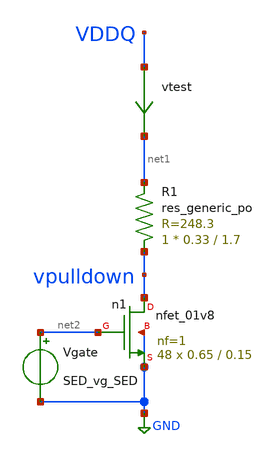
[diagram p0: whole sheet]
** sch_path: schem/test_pd_res.sch
* Copyright 2021 Stefan Frederik Schippers
* Licensed under the Apache License, Version 2.0 (the "License");
* you may not use this file except in compliance with the License.
* You may obtain a copy of the License at
* https://www.apache.org/licenses/LICENSE-2.0
* Unless required by applicable law or agreed to in writing, software
* distributed under the License is distributed on an "AS IS" BASIS,
* WITHOUT WARRANTIES OR CONDITIONS OF ANY KIND, either express or implied.
* See the License for the specific language governing permissions and
* limitations under the License.
**.subckt test_pd_res
XR1 vpulldown net1 sky130_fd_pr__res_generic_po W=0.33 L=1.7 m=1
vtest VDDQ net1 0
.save i(vtest)
Xn1 vpulldown net2 GND GND sky130_fd_pr__nfet_01v8 L=0.15 W=0.65 nf=1 ad='int((nf+1)/2) * W/nf * 0.29'
+ as='int((nf+2)/2) * W/nf * 0.29' pd='2*int((nf+1)/2) * (W/nf + 0.29)' ps='2*int((nf+2)/2) * (W/nf + 0.29)'
+ nrd='0.29 / W' nrs='0.29 / W' sa=0 sb=0 sd=0 mult=48 m=48
Vgate net2 GND SED_vg_SED
**** begin user architecture code
 ** Local library links to pdk
.lib ./sky130/libs/SED_process_SED_lib.spice SED_process_SED

**** end user architecture code
**.ends
.GLOBAL GND
**** begin user architecture code



* power voltage
vvddq VDDQ 0 0

.control
save all
set temp=SED_temp_SED

* RUN SIMULATION
dc vvddq 0.3 1.2 0.05
* OUTPUT
print v(vddq)/i(vtest)
wrdata out/SED_outName_SED/SED_plotName_SED.txt v(vddq)/i(vtest)
set hcopydevtype = svg
hardcopy ./out/SED_outName_SED/SED_plotName_SED.svg vddq/I(vtest) vs vddq title 'Resistance vs pin voltage'

.endc


**** end user architecture code
.end
